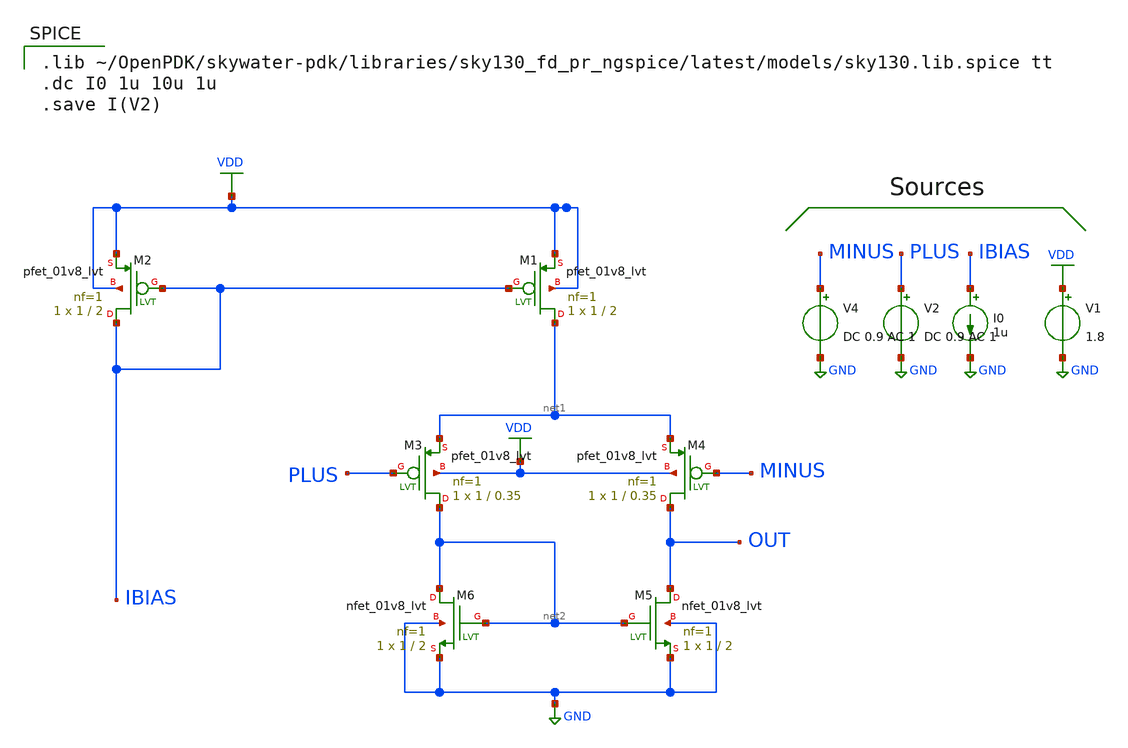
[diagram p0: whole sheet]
** sch_path: xschem/MISC/TL_OPAMP.sch
**.subckt TL_OPAMP
XM1 net1 IBIAS VDD VDD sky130_fd_pr__pfet_01v8_lvt L=2 W=1 nf=1 ad='int((nf+1)/2) * W/nf * 0.29' as='int((nf+2)/2) * W/nf * 0.29'
+ pd='2*int((nf+1)/2) * (W/nf + 0.29)' ps='2*int((nf+2)/2) * (W/nf + 0.29)' nrd='0.29 / W' nrs='0.29 / W'
+ sa=0 sb=0 sd=0 mult=1 m=1
XM2 IBIAS IBIAS VDD VDD sky130_fd_pr__pfet_01v8_lvt L=2 W=1 nf=1 ad='int((nf+1)/2) * W/nf * 0.29' as='int((nf+2)/2) * W/nf * 0.29'
+ pd='2*int((nf+1)/2) * (W/nf + 0.29)' ps='2*int((nf+2)/2) * (W/nf + 0.29)' nrd='0.29 / W' nrs='0.29 / W'
+ sa=0 sb=0 sd=0 mult=1 m=1
I0 IBIAS GND 1u
V1 VDD GND 1.8
XM3 net2 PLUS net1 VDD sky130_fd_pr__pfet_01v8_lvt L=0.35 W=1 nf=1 ad='int((nf+1)/2) * W/nf * 0.29' as='int((nf+2)/2) * W/nf * 0.29'
+ pd='2*int((nf+1)/2) * (W/nf + 0.29)' ps='2*int((nf+2)/2) * (W/nf + 0.29)' nrd='0.29 / W' nrs='0.29 / W'
+ sa=0 sb=0 sd=0 mult=1 m=1
XM4 OUT MINUS net1 VDD sky130_fd_pr__pfet_01v8_lvt L=0.35 W=1 nf=1 ad='int((nf+1)/2) * W/nf * 0.29' as='int((nf+2)/2) * W/nf * 0.29'
+ pd='2*int((nf+1)/2) * (W/nf + 0.29)' ps='2*int((nf+2)/2) * (W/nf + 0.29)' nrd='0.29 / W' nrs='0.29 / W'
+ sa=0 sb=0 sd=0 mult=1 m=1
XM5 OUT net2 GND GND sky130_fd_pr__nfet_01v8_lvt L=2 W=1 nf=1 ad='int((nf+1)/2) * W/nf * 0.29' as='int((nf+2)/2) * W/nf * 0.29'
+ pd='2*int((nf+1)/2) * (W/nf + 0.29)' ps='2*int((nf+2)/2) * (W/nf + 0.29)' nrd='0.29 / W' nrs='0.29 / W'
+ sa=0 sb=0 sd=0 mult=1 m=1
XM6 net2 net2 GND GND sky130_fd_pr__nfet_01v8_lvt L=2 W=1 nf=1 ad='int((nf+1)/2) * W/nf * 0.29' as='int((nf+2)/2) * W/nf * 0.29'
+ pd='2*int((nf+1)/2) * (W/nf + 0.29)' ps='2*int((nf+2)/2) * (W/nf + 0.29)' nrd='0.29 / W' nrs='0.29 / W'
+ sa=0 sb=0 sd=0 mult=1 m=1
V2 PLUS GND DC 0.9 AC 1
V4 MINUS GND DC 0.9 AC 1
**** begin user architecture code

.lib ~/OpenPDK/skywater-pdk/libraries/sky130_fd_pr_ngspice/latest/models/sky130.lib.spice tt
.dc I0 1u 10u 1u
.save I(V2)

**** end user architecture code
**.ends
.GLOBAL GND
.GLOBAL VDD
.end
